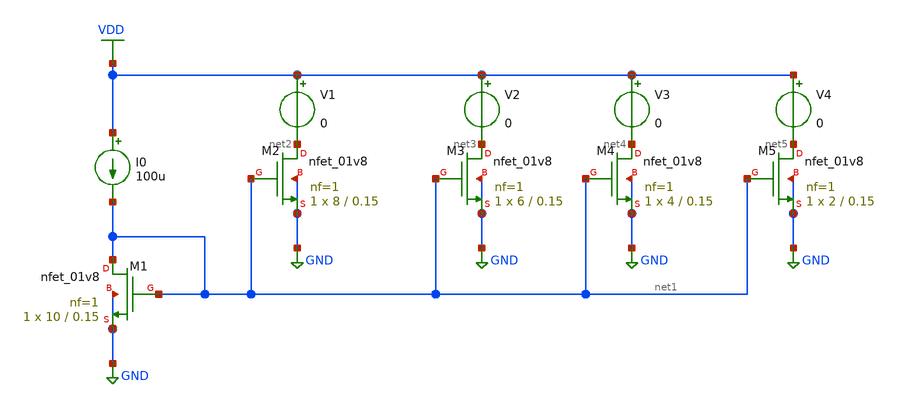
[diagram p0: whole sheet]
** sch_path: Neuron/ultralif/untitled-1.sch
**.subckt untitled-1
XM2 net2 net1 GND GND sky130_fd_pr__nfet_01v8 L=0.15 W=8 nf=1 ad='int((1 + 1)/2) * 8 / 1 * 0.29' as='int((1 + 2)/2) * 8 / 1 * 0.29'
+ pd='2*int((1 + 1)/2) * (8 / 1 + 0.29)' ps='2*int((1 + 2)/2) * (8 / 1 + 0.29)' nrd='0.29 / 8 ' nrs='0.29 / 8 '
+ sa=0 sb=0 sd=0 mult=1 m=1
XM1 net1 net1 GND GND sky130_fd_pr__nfet_01v8 L=0.15 W=10 nf=1 ad='int((1 + 1)/2) * 10 / 1 * 0.29' as='int((1 + 2)/2) * 10 / 1 * 0.29'
+ pd='2*int((1 + 1)/2) * (10 / 1 + 0.29)' ps='2*int((1 + 2)/2) * (10 / 1 + 0.29)' nrd='0.29 / 10 ' nrs='0.29 / 10 '
+ sa=0 sb=0 sd=0 mult=1 m=1
I0 VDD net1 100u
V1 VDD net2 0
XM3 net3 net1 GND GND sky130_fd_pr__nfet_01v8 L=0.15 W=6 nf=1 ad='int((1 + 1)/2) * 6 / 1 * 0.29' as='int((1 + 2)/2) * 6 / 1 * 0.29'
+ pd='2*int((1 + 1)/2) * (6 / 1 + 0.29)' ps='2*int((1 + 2)/2) * (6 / 1 + 0.29)' nrd='0.29 / 6 ' nrs='0.29 / 6 '
+ sa=0 sb=0 sd=0 mult=1 m=1
V2 VDD net3 0
XM4 net4 net1 GND GND sky130_fd_pr__nfet_01v8 L=0.15 W=4 nf=1 ad='int((1 + 1)/2) * 4 / 1 * 0.29' as='int((1 + 2)/2) * 4 / 1 * 0.29'
+ pd='2*int((1 + 1)/2) * (4 / 1 + 0.29)' ps='2*int((1 + 2)/2) * (4 / 1 + 0.29)' nrd='0.29 / 4 ' nrs='0.29 / 4 '
+ sa=0 sb=0 sd=0 mult=1 m=1
V3 VDD net4 0
XM5 net5 net1 GND GND sky130_fd_pr__nfet_01v8 L=0.15 W=2 nf=1 ad='int((1 + 1)/2) * 2 / 1 * 0.29' as='int((1 + 2)/2) * 2 / 1 * 0.29'
+ pd='2*int((1 + 1)/2) * (2 / 1 + 0.29)' ps='2*int((1 + 2)/2) * (2 / 1 + 0.29)' nrd='0.29 / 2 ' nrs='0.29 / 2 '
+ sa=0 sb=0 sd=0 mult=1 m=1
V4 VDD net5 0
**** begin user architecture code

** opencircuitdesign pdks install
.lib $::SKYWATER_MODELS/sky130.lib.spice tt


**** end user architecture code
**.ends
.GLOBAL GND
.GLOBAL VDD
.end
